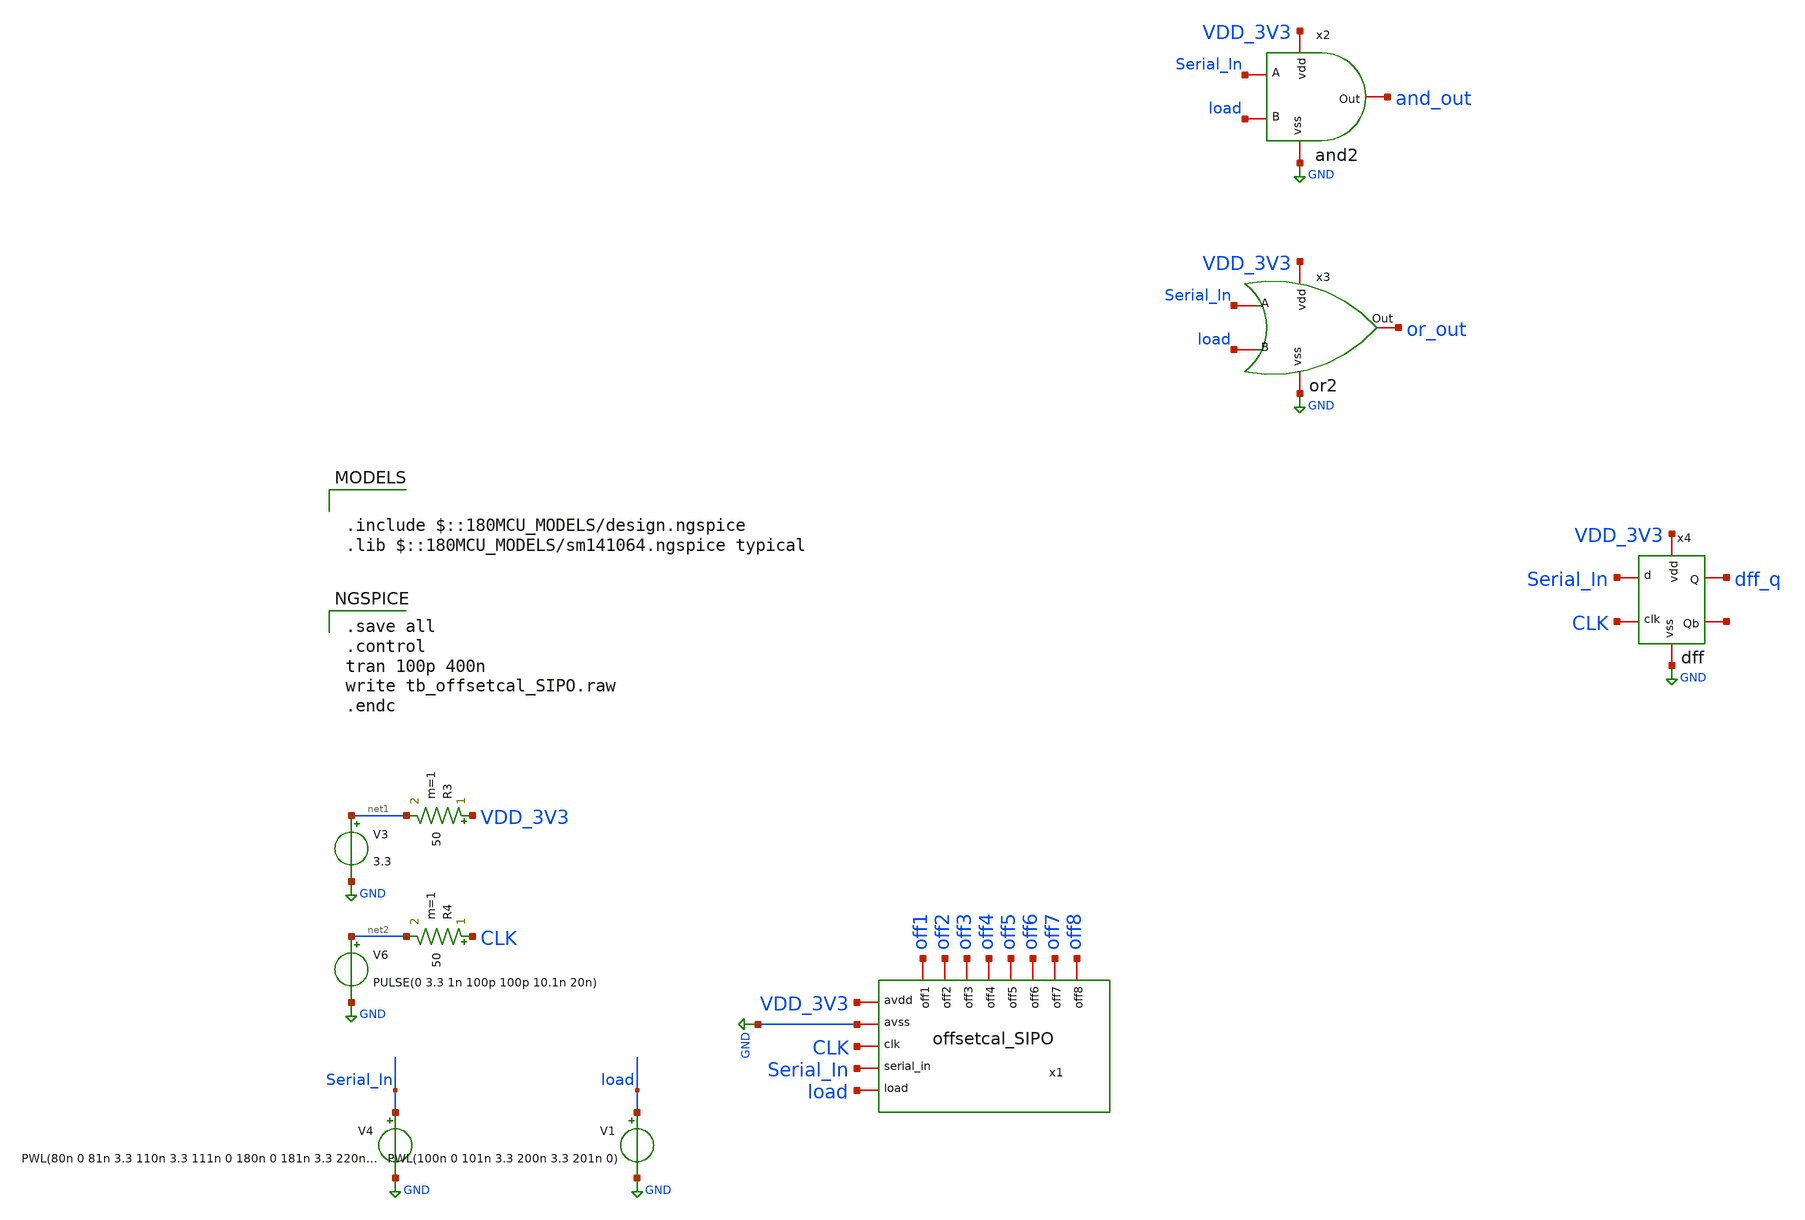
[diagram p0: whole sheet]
** sch_path: designs/libs/SIPO/tb_offsetcal_SIPO.sch
**.subckt tb_offsetcal_SIPO
x1 VDD_3V3 GND off4 off2 off6 off5 off1 off7 off8 off3 Serial_In CLK load offsetcal_SIPO
V3 net1 GND 3.3
V6 net2 GND PULSE(0 3.3 1n 100p 100p 10.1n 20n)
R3 VDD_3V3 net1 50 m=1
R4 CLK net2 50 m=1
V4 Serial_In GND PWL(80n 0 81n 3.3 110n 3.3 111n 0 180n 0 181n 3.3 220n 3.3 221n 0)
V1 load GND PWL(100n 0 101n 3.3 200n 3.3 201n 0)
x2 VDD_3V3 load Serial_In and_out GND and2
x3 VDD_3V3 or_out load Serial_In GND or2
x4 Serial_In dff_q VDD_3V3 GND CLK net3 dff
**** begin user architecture code

.include $::180MCU_MODELS/design.ngspice
.lib $::180MCU_MODELS/sm141064.ngspice typical


.save all
.control
tran 100p 400n
write tb_offsetcal_SIPO.raw
.endc

**** end user architecture code
**.ends
.GLOBAL GND
.end
